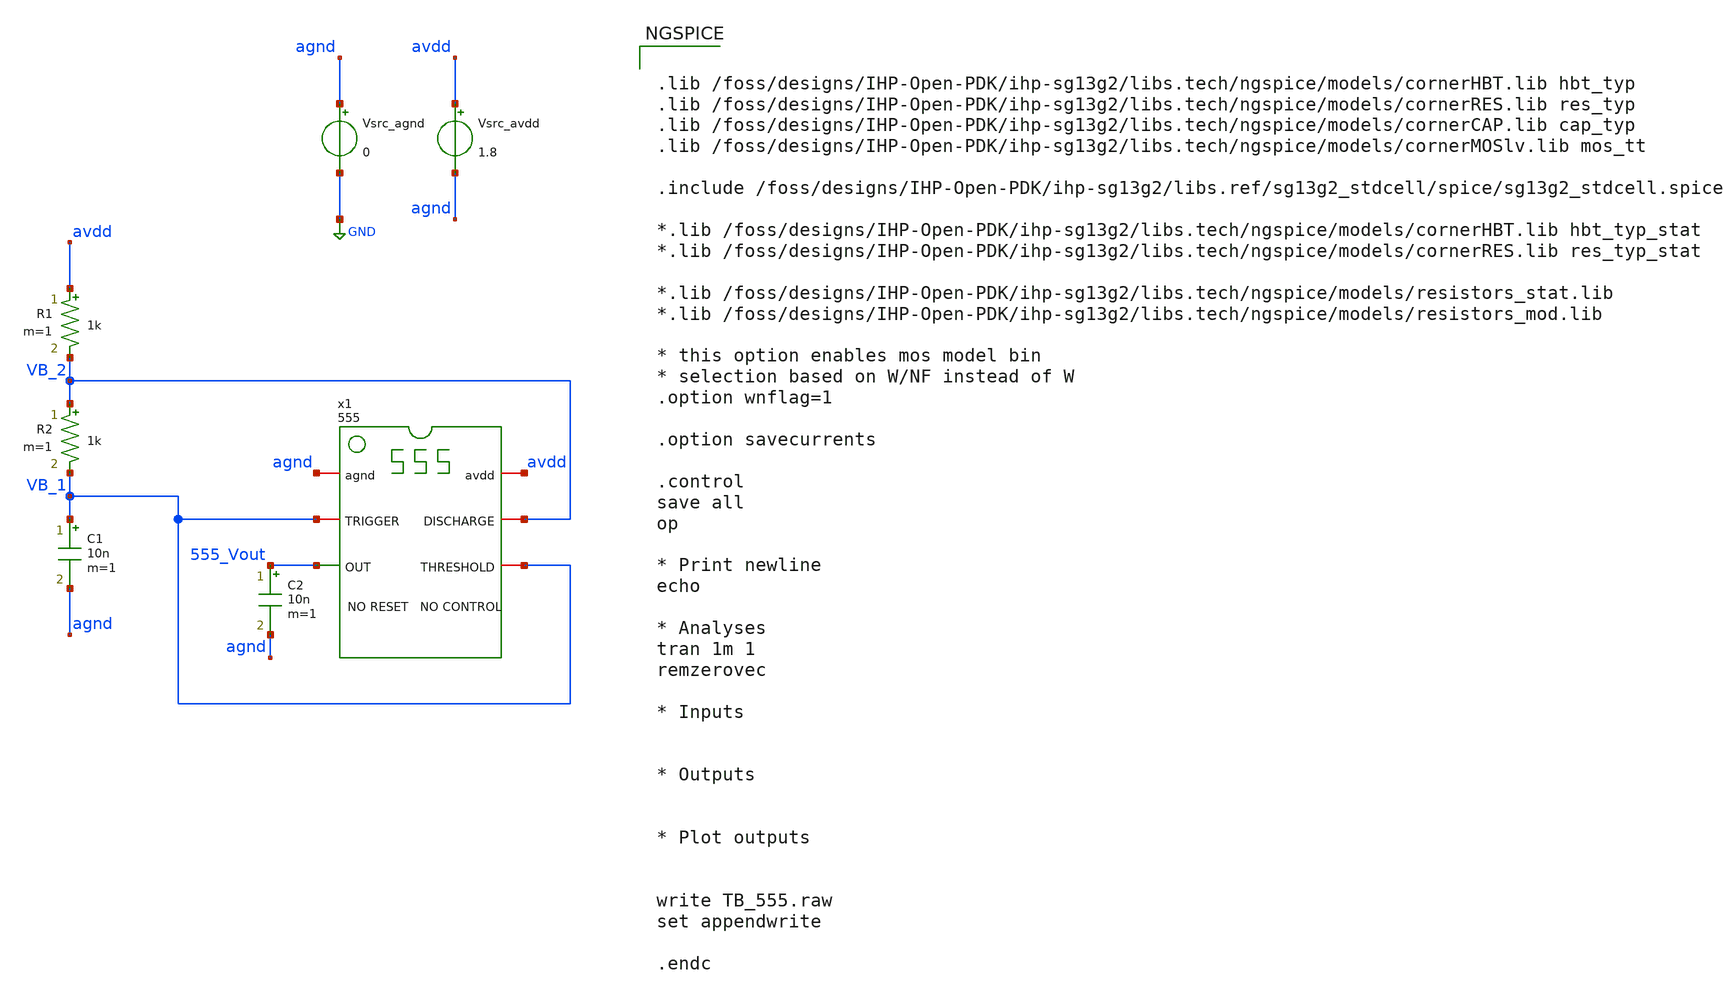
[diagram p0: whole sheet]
** sch_path: xschem/TB_555.sch
**.subckt TB_555
x1 avdd VB_1 555_Vout VB_2 VB_1 agnd 555
Vsrc_agnd agnd GND 0
Vsrc_avdd avdd agnd 1.8
C1 VB_1 agnd 10n m=1
R1 avdd VB_2 1k m=1
R2 VB_2 VB_1 1k m=1
C2 555_Vout agnd 10n m=1
**** begin user architecture code


.lib /foss/designs/IHP-Open-PDK/ihp-sg13g2/libs.tech/ngspice/models/cornerHBT.lib hbt_typ
.lib /foss/designs/IHP-Open-PDK/ihp-sg13g2/libs.tech/ngspice/models/cornerRES.lib res_typ
.lib /foss/designs/IHP-Open-PDK/ihp-sg13g2/libs.tech/ngspice/models/cornerCAP.lib cap_typ
.lib /foss/designs/IHP-Open-PDK/ihp-sg13g2/libs.tech/ngspice/models/cornerMOSlv.lib mos_tt

.include /foss/designs/IHP-Open-PDK/ihp-sg13g2/libs.ref/sg13g2_stdcell/spice/sg13g2_stdcell.spice

*.lib /foss/designs/IHP-Open-PDK/ihp-sg13g2/libs.tech/ngspice/models/cornerHBT.lib hbt_typ_stat
*.lib /foss/designs/IHP-Open-PDK/ihp-sg13g2/libs.tech/ngspice/models/cornerRES.lib res_typ_stat

*.lib /foss/designs/IHP-Open-PDK/ihp-sg13g2/libs.tech/ngspice/models/resistors_stat.lib
*.lib /foss/designs/IHP-Open-PDK/ihp-sg13g2/libs.tech/ngspice/models/resistors_mod.lib

* this option enables mos model bin
* selection based on W/NF instead of W
.option wnflag=1

.option savecurrents

.control
save all
op

* Print newline
echo

* Analyses
tran 1m 1
remzerovec

* Inputs


* Outputs


* Plot outputs


write TB_555.raw
set appendwrite

.endc


**** end user architecture code
**.ends

* expanding   symbol:  555.sym # of pins=6
** sym_path: xschem/555.sym
** sch_path: xschem/555.sch
.subckt 555 avdd THRESHOLD OUT DISCHARGE TRIGGER agnd
*.opin OUT
*.iopin avdd
*.iopin agnd
*.iopin TRIGGER
*.iopin THRESHOLD
*.iopin DISCHARGE
XR3 avdd VB_2 sub! rhigh w=0.5e-6 l=1.59e-6 m=1 b=0 mm_ok=1
XR1 VB_1 agnd sub! rhigh w=0.5e-6 l=1.59e-6 m=1 b=0 mm_ok=1
XR2 VB_2 VB_1 sub! rhigh w=0.5e-6 l=1.59e-6 m=1 b=0 mm_ok=1
XC1 VB_1 agnd cap_cmim w=7.0e-6 l=7.0e-6 m=1 mm_ok=1
XC2 VB_2 agnd cap_cmim w=7.0e-6 l=7.0e-6 m=1 mm_ok=1
XC3 avdd agnd cap_cmim w=7.0e-6 l=7.0e-6 m=1 mm_ok=1
XR4 net8 out_bar sub! rhigh w=0.5e-6 l=1.59e-6 m=1 b=0 mm_ok=1
x1 avdd net2 net9 VB_2 THRESHOLD agnd comparator
x2 avdd net1 net10 TRIGGER VB_1 agnd comparator
x9 avdd net2 net4 agnd buffer
x10 avdd net1 net3 agnd buffer
x3 avdd net6 net5 agnd net3 net4 SR_latch
x4 avdd net5 OUT agnd buffer
x5 avdd net6 out_bar agnd buffer
* noconn #net9
* noconn #net10
XQ1 DISCHARGE net8 net7 agnd npn13G2 Nx=1 mm_ok=1
XR5 net7 agnd sub! rppd w=1e-6 l=0.5e-6 m=1 b=0 mm_ok=1
.ends


* expanding   symbol:  comparator.sym # of pins=6
** sym_path: xschem/comparator.sym
** sch_path: xschem/comparator.sch
.subckt comparator avdd voutp voutn vinn vinp agnd
*.iopin avdd
*.ipin vinp
*.opin voutp
*.iopin agnd
*.ipin vinn
*.opin voutn
XQ1 voutp vinn net1 agnd npn13G2 Nx=1 mm_ok=1
XR1 avdd voutp sub! rppd w=0.5e-6 l=7.5e-6 m=1 b=0 mm_ok=1
XR2 net1 agnd sub! rppd w=0.5e-6 l=0.5e-6 m=1 b=0 mm_ok=1
XR3 avdd voutn sub! rppd w=0.5e-6 l=7.5e-6 m=1 b=0 mm_ok=1
XQ2 voutn vinp net1 agnd npn13G2 Nx=1 mm_ok=1
.ends


* expanding   symbol:  buffer.sym # of pins=4
** sym_path: xschem/buffer.sym
** sch_path: xschem/buffer.sch
.subckt buffer avdd vin vout agnd
*.iopin avdd
*.ipin vin
*.opin vout
*.iopin agnd
x1 avdd vin net1 agnd inverter
x2 avdd net1 vout agnd inverter
.ends


* expanding   symbol:  SR_latch.sym # of pins=6
** sym_path: xschem/SR_latch.sym
** sch_path: xschem/SR_latch.sch
.subckt SR_latch avdd Q_bar Q agnd S R
*.ipin R
*.opin Q_bar
*.ipin S
*.opin Q
*.iopin avdd
*.iopin agnd
XQ2 Q_bar net2 agnd agnd npn13G2 Nx=1 mm_ok=1
XQ1 Q net1 agnd agnd npn13G2 Nx=1 mm_ok=1
XR3 net1 R sub! rppd w=0.5e-6 l=20e-6 m=1 b=0 mm_ok=1
XR1 S net2 sub! rppd w=0.5e-6 l=20e-6 m=1 b=0 mm_ok=1
XR2 net1 agnd sub! rhigh w=0.5e-6 l=20e-6 m=1 b=0 mm_ok=1
XR4 net2 agnd sub! rhigh w=0.5e-6 l=20e-6 m=1 b=0 mm_ok=1
XR5 net2 Q sub! rppd w=0.5e-6 l=20e-6 m=1 b=0 mm_ok=1
XR6 Q_bar net1 sub! rppd w=0.5e-6 l=20e-6 m=1 b=0 mm_ok=1
XR7 avdd Q sub! rppd w=0.5e-6 l=2e-6 m=1 b=0 mm_ok=1
XR8 avdd Q_bar sub! rppd w=0.5e-6 l=2e-6 m=1 b=0 mm_ok=1
.ends


* expanding   symbol:  inverter.sym # of pins=4
** sym_path: xschem/inverter.sym
** sch_path: xschem/inverter.sch
.subckt inverter avdd vin vout agnd
*.iopin avdd
*.ipin vin
*.opin vout
*.iopin agnd
XQ1 vout base agnd agnd npn13G2 Nx=10 mm_ok=1
XR1 avdd vout sub! rhigh w=1e-6 l=0.5e-6 m=1 b=0 mm_ok=1
XR2 base vin sub! rhigh w=0.5e-6 l=0.5e-6 m=1 b=0 mm_ok=1
.ends

.GLOBAL GND
.end
